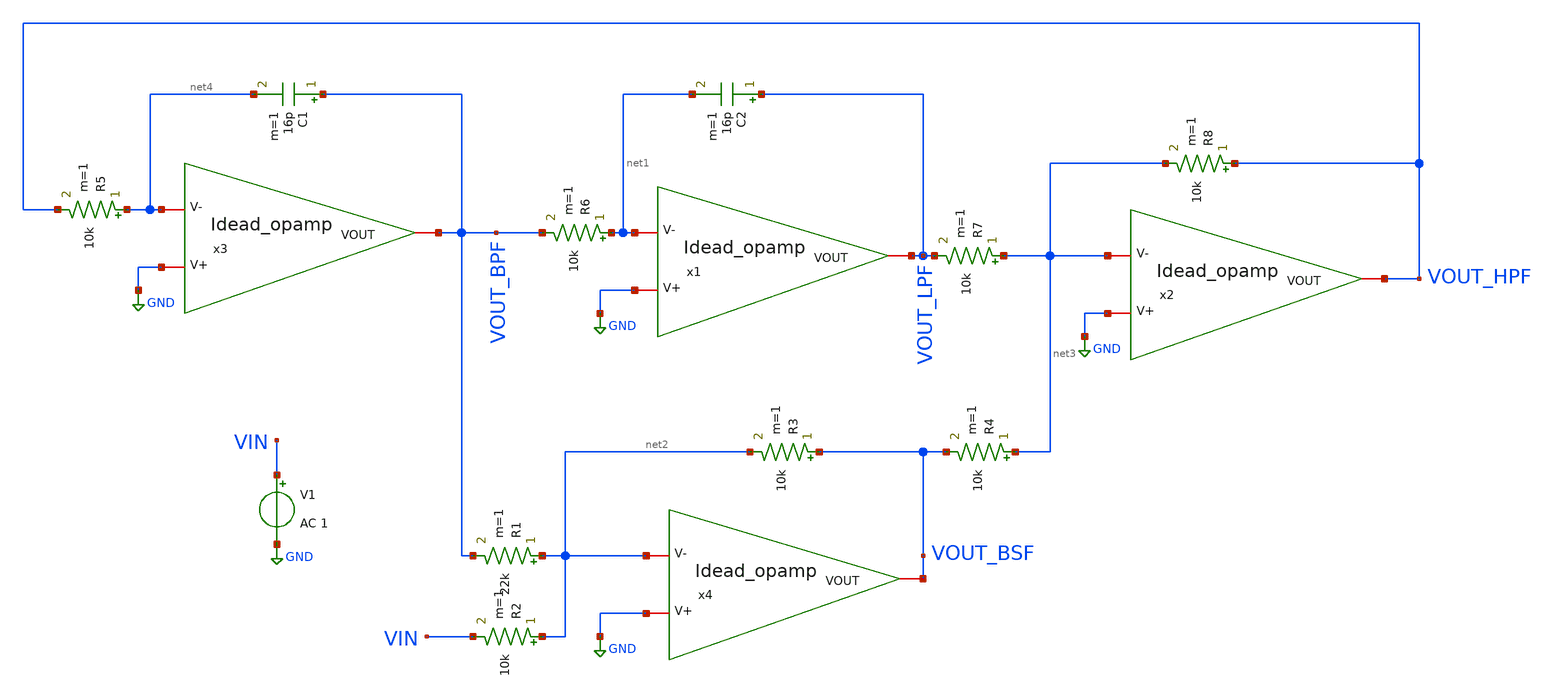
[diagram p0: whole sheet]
** sch_path: Design/Testbench.sch
**.subckt Testbench
x1 VOUT_LPF net1 GND Idead_opamp
x2 VOUT_HPF net3 GND Idead_opamp
x3 VOUT_BPF net4 GND Idead_opamp
x4 VOUT_BSF net2 GND Idead_opamp
R1 net2 VOUT_BPF 22k m=1
C1 VOUT_BPF net4 16p m=1
R2 net2 VIN 10k m=1
R3 VOUT_BSF net2 10k m=1
R4 net3 VOUT_BSF 10k m=1
R5 net4 VOUT_HPF 10k m=1
R6 net1 VOUT_BPF 10k m=1
R7 net3 VOUT_LPF 10k m=1
R8 VOUT_HPF net3 10k m=1
C2 VOUT_LPF net1 16p m=1
V1 VIN GND AC 1
**** begin user architecture code

.include sim_script.sim

**** end user architecture code
**.ends

* expanding   symbol:  Idead_opamp.sym # of pins=3
** sym_path: Design/Idead_opamp.sym
** sch_path: Design/Idead_opamp.sch
.subckt Idead_opamp VOUT V- V+
*.iopin V-
*.iopin V+
*.iopin VOUT
E1 VOUT1 GND V+ V- 10000
B1 VOUT GND V = max(-1, min(1, V(VOUT1)))
.ends

.GLOBAL GND
.end
